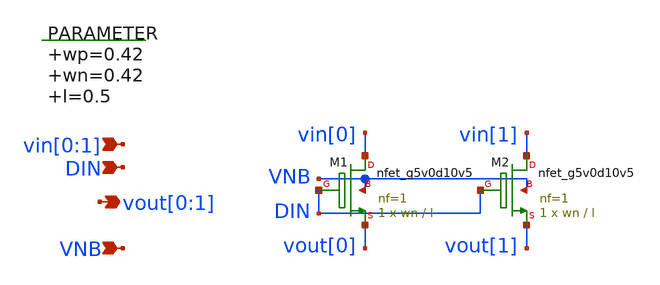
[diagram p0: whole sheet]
** sch_path: xschem/switch_nmos_1g_2o.sch
**.subckt switch_nmos_1g_2o vin[0],vin[1] vout[0],vout[1] VNB DIN
*.ipin vin[0],vin[1]
*.opin vout[0],vout[1]
*.ipin VNB
*.ipin DIN
.param wp=0.42 wn=0.42 l=0.5

XM1 vin[0] DIN vout[0] VNB sky130_fd_pr__nfet_g5v0d10v5 L=l W=wn nf=1 ad='int((nf+1)/2) * W/nf * 0.29'
+ as='int((nf+2)/2) * W/nf * 0.29' pd='2*int((nf+1)/2) * (W/nf + 0.29)' ps='2*int((nf+2)/2) * (W/nf + 0.29)'
+ nrd='0.29 / W' nrs='0.29 / W' sa=0 sb=0 sd=0 mult=1 m=1
XM2 vin[1] DIN vout[1] VNB sky130_fd_pr__nfet_g5v0d10v5 L=l W=wn nf=1 ad='int((nf+1)/2) * W/nf * 0.29'
+ as='int((nf+2)/2) * W/nf * 0.29' pd='2*int((nf+1)/2) * (W/nf + 0.29)' ps='2*int((nf+2)/2) * (W/nf + 0.29)'
+ nrd='0.29 / W' nrs='0.29 / W' sa=0 sb=0 sd=0 mult=1 m=1
**.ends
.end
